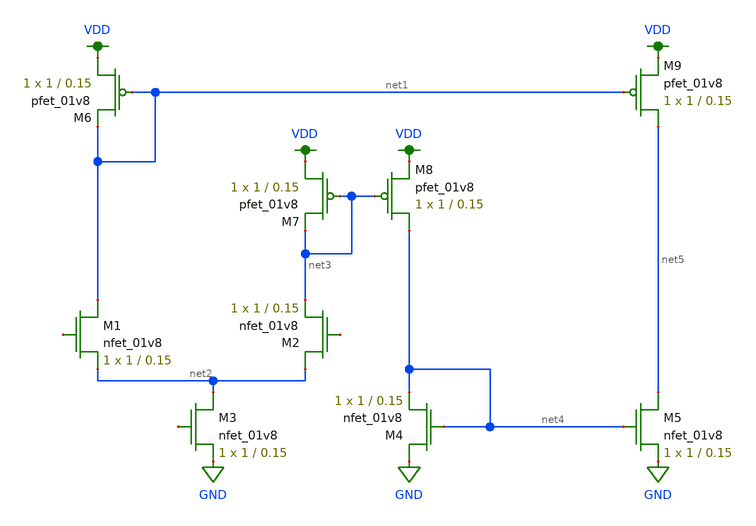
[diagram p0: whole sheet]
** sch_path: schematic/nmos_current_mirror_diff_amp.sch
**.subckt nmos_current_mirror_diff_amp
XM1 net1 net6 net2 GND sky130_fd_pr__nfet_01v8 L=0.15 W=1 nf=1 ad='int((nf+1)/2) * W/nf * 0.29' as='int((nf+2)/2) * W/nf * 0.29'
+ pd='2*int((nf+1)/2) * (W/nf + 0.29)' ps='2*int((nf+2)/2) * (W/nf + 0.29)' nrd='0.29 / W' nrs='0.29 / W'
+ sa=0 sb=0 sd=0 mult=1 m=1
XM2 net2 net7 net3 GND sky130_fd_pr__nfet_01v8 L=0.15 W=1 nf=1 ad='int((nf+1)/2) * W/nf * 0.29' as='int((nf+2)/2) * W/nf * 0.29'
+ pd='2*int((nf+1)/2) * (W/nf + 0.29)' ps='2*int((nf+2)/2) * (W/nf + 0.29)' nrd='0.29 / W' nrs='0.29 / W'
+ sa=0 sb=0 sd=0 mult=1 m=1
XM3 net2 net8 GND GND sky130_fd_pr__nfet_01v8 L=0.15 W=1 nf=1 ad='int((nf+1)/2) * W/nf * 0.29' as='int((nf+2)/2) * W/nf * 0.29'
+ pd='2*int((nf+1)/2) * (W/nf + 0.29)' ps='2*int((nf+2)/2) * (W/nf + 0.29)' nrd='0.29 / W' nrs='0.29 / W'
+ sa=0 sb=0 sd=0 mult=1 m=1
XM4 GND net4 net4 GND sky130_fd_pr__nfet_01v8 L=0.15 W=1 nf=1 ad='int((nf+1)/2) * W/nf * 0.29' as='int((nf+2)/2) * W/nf * 0.29'
+ pd='2*int((nf+1)/2) * (W/nf + 0.29)' ps='2*int((nf+2)/2) * (W/nf + 0.29)' nrd='0.29 / W' nrs='0.29 / W'
+ sa=0 sb=0 sd=0 mult=1 m=1
XM5 net5 net4 GND GND sky130_fd_pr__nfet_01v8 L=0.15 W=1 nf=1 ad='int((nf+1)/2) * W/nf * 0.29' as='int((nf+2)/2) * W/nf * 0.29'
+ pd='2*int((nf+1)/2) * (W/nf + 0.29)' ps='2*int((nf+2)/2) * (W/nf + 0.29)' nrd='0.29 / W' nrs='0.29 / W'
+ sa=0 sb=0 sd=0 mult=1 m=1
XM6 VDD net1 net1 VDD sky130_fd_pr__pfet_01v8 L=0.15 W=1 nf=1 ad='int((nf+1)/2) * W/nf * 0.29' as='int((nf+2)/2) * W/nf * 0.29'
+ pd='2*int((nf+1)/2) * (W/nf + 0.29)' ps='2*int((nf+2)/2) * (W/nf + 0.29)' nrd='0.29 / W' nrs='0.29 / W'
+ sa=0 sb=0 sd=0 mult=1 m=1
XM7 VDD net3 net3 VDD sky130_fd_pr__pfet_01v8 L=0.15 W=1 nf=1 ad='int((nf+1)/2) * W/nf * 0.29' as='int((nf+2)/2) * W/nf * 0.29'
+ pd='2*int((nf+1)/2) * (W/nf + 0.29)' ps='2*int((nf+2)/2) * (W/nf + 0.29)' nrd='0.29 / W' nrs='0.29 / W'
+ sa=0 sb=0 sd=0 mult=1 m=1
XM8 net4 net3 VDD VDD sky130_fd_pr__pfet_01v8 L=0.15 W=1 nf=1 ad='int((nf+1)/2) * W/nf * 0.29' as='int((nf+2)/2) * W/nf * 0.29'
+ pd='2*int((nf+1)/2) * (W/nf + 0.29)' ps='2*int((nf+2)/2) * (W/nf + 0.29)' nrd='0.29 / W' nrs='0.29 / W'
+ sa=0 sb=0 sd=0 mult=1 m=1
XM9 net5 net1 VDD VDD sky130_fd_pr__pfet_01v8 L=0.15 W=1 nf=1 ad='int((nf+1)/2) * W/nf * 0.29' as='int((nf+2)/2) * W/nf * 0.29'
+ pd='2*int((nf+1)/2) * (W/nf + 0.29)' ps='2*int((nf+2)/2) * (W/nf + 0.29)' nrd='0.29 / W' nrs='0.29 / W'
+ sa=0 sb=0 sd=0 mult=1 m=1
**.ends
.GLOBAL GND
.GLOBAL VDD
.end
